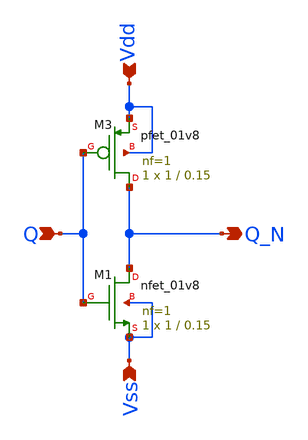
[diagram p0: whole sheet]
** sch_path: Behavioral_model/CMOS_inverter.sch
**.subckt CMOS_inverter Q Vdd Vss Q_N
*.ipin Q
*.ipin Vdd
*.ipin Vss
*.opin Q_N
XM1 Q_N Q Vss Vss sky130_fd_pr__nfet_01v8 L=0.15 W=1 nf=1 ad='int((nf+1)/2) * W/nf * 0.29' as='int((nf+2)/2) * W/nf * 0.29'
+ pd='2*int((nf+1)/2) * (W/nf + 0.29)' ps='2*int((nf+2)/2) * (W/nf + 0.29)' nrd='0.29 / W' nrs='0.29 / W'
+ sa=0 sb=0 sd=0 mult=1 m=1
XM3 Q_N Q Vdd Vdd sky130_fd_pr__pfet_01v8 L=0.15 W=1 nf=1 ad='int((nf+1)/2) * W/nf * 0.29' as='int((nf+2)/2) * W/nf * 0.29'
+ pd='2*int((nf+1)/2) * (W/nf + 0.29)' ps='2*int((nf+2)/2) * (W/nf + 0.29)' nrd='0.29 / W' nrs='0.29 / W'
+ sa=0 sb=0 sd=0 mult=1 m=1
**.ends
.end
